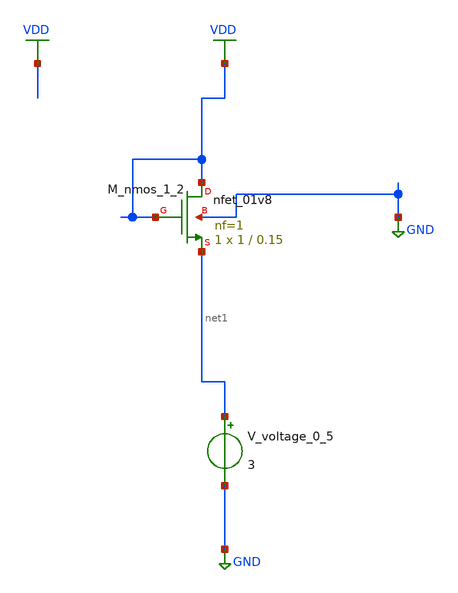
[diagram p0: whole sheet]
** sch_path: schematics/AMSNet/73.sch
**.subckt 73
XM_nmos_1_2 VDD VDD net1 GND sky130_fd_pr__nfet_01v8 L=0.15 W=1 nf=1 ad='int((1 + 1)/2) * 1 / 1 * 0.29'
+ as='int((1 + 2)/2) * 1 / 1 * 0.29' pd='2*int((1 + 1)/2) * (1 / 1 + 0.29)' ps='2*int((1 + 2)/2) * (1 / 1 + 0.29)'
+ nrd='0.29 / 1 ' nrs='0.29 / 1 ' sa=0 sb=0 sd=0 mult=1 m=1
V_voltage_0_5 net1 GND 3
**.ends
.GLOBAL GND
.GLOBAL VDD
.end
